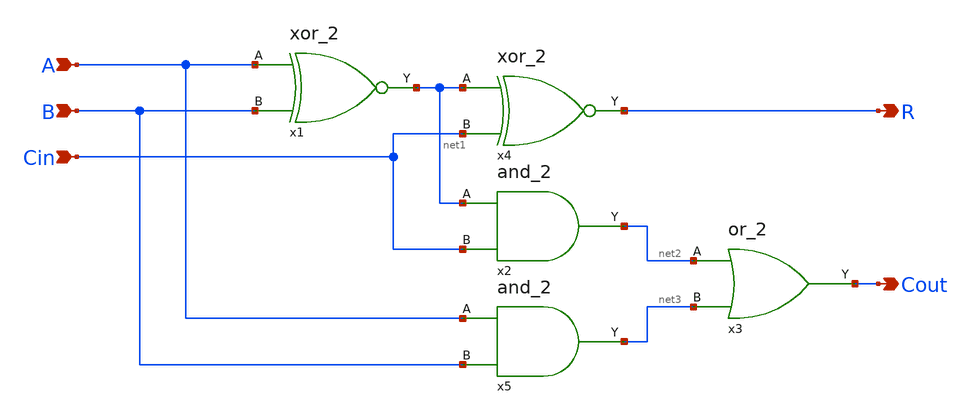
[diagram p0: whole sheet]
** sch_path: Circuiti/multiplier/full_adder.sch
**.subckt full_adder A B Cin R Cout
*.ipin A
*.ipin B
*.ipin Cin
*.opin R
*.opin Cout
x1 A net1 B xor_2
x2 net1 net2 Cin and_2
x3 net2 Cout net3 or_2
x4 net1 R Cin xor_2
x5 A net3 B and_2
**.ends

* expanding   symbol:  /home/matteo/Documenti/tesi/Circuiti/logic_gates_sch_sym/xor_2.sym # of
*+ pins=3
** sym_path: Circuiti/logic_gates_sch_sym/xor_2.sym
** sch_path: Circuiti/logic_gates_sch_sym/xor_2.sch
.subckt xor_2 A Y B
*.ipin A
*.ipin B
*.opin Y
x1 A net1 B nand_2
x2 A net2 B or_2
x3 net1 Y net2 and_2
.ends


* expanding   symbol:  /home/matteo/Documenti/tesi/Circuiti/logic_gates_sch_sym/and_2.sym # of
*+ pins=3
** sym_path: Circuiti/logic_gates_sch_sym/and_2.sym
** sch_path: Circuiti/logic_gates_sch_sym/and_2.sch
.subckt and_2 A Y B
*.ipin B
*.ipin A
*.opin Y
x1 A net1 B nand_2
x2 net1 Y not
.ends


* expanding   symbol:  /home/matteo/Documenti/tesi/Circuiti/logic_gates_sch_sym/or_2.sym # of pins=3
** sym_path: Circuiti/logic_gates_sch_sym/or_2.sym
** sch_path: Circuiti/logic_gates_sch_sym/or_2.sch
.subckt or_2 A Y B
*.ipin A
*.ipin B
*.opin Y
x1 A net1 B nor_2
x2 net1 Y not
.ends


* expanding   symbol:  /home/matteo/Documenti/tesi/Circuiti/logic_gates_sch_sym/nand_2.sym # of
*+ pins=3
** sym_path: Circuiti/logic_gates_sch_sym/nand_2.sym
** sch_path: Circuiti/logic_gates_sch_sym/nand_2.sch
.subckt nand_2 A Y B
*.ipin A
*.ipin B
*.opin Y
XM1 Y A net1 GND sky130_fd_pr__nfet_01v8 L=0.15 W=1 nf=1 ad='int((nf+1)/2) * W/nf * 0.29' as='int((nf+2)/2) * W/nf * 0.29'
+ pd='2*int((nf+1)/2) * (W/nf + 0.29)' ps='2*int((nf+2)/2) * (W/nf + 0.29)' nrd='0.29 / W' nrs='0.29 / W'
+ sa=0 sb=0 sd=0 mult=1 m=1
XM3 Y B Vdd VDD sky130_fd_pr__pfet_01v8 L=0.45 W=4.8 nf=1 ad='int((nf+1)/2) * W/nf * 0.29' as='int((nf+2)/2) * W/nf * 0.29'
+ pd='2*int((nf+1)/2) * (W/nf + 0.29)' ps='2*int((nf+2)/2) * (W/nf + 0.29)' nrd='0.29 / W' nrs='0.29 / W'
+ sa=0 sb=0 sd=0 mult=1 m=1
XM4 Y A Vdd VDD sky130_fd_pr__pfet_01v8 L=0.45 W=4.8 nf=1 ad='int((nf+1)/2) * W/nf * 0.29' as='int((nf+2)/2) * W/nf * 0.29'
+ pd='2*int((nf+1)/2) * (W/nf + 0.29)' ps='2*int((nf+2)/2) * (W/nf + 0.29)' nrd='0.29 / W' nrs='0.29 / W'
+ sa=0 sb=0 sd=0 mult=1 m=1
XM2 net1 B GND GND sky130_fd_pr__nfet_01v8 L=0.15 W=1 nf=1 ad='int((nf+1)/2) * W/nf * 0.29' as='int((nf+2)/2) * W/nf * 0.29'
+ pd='2*int((nf+1)/2) * (W/nf + 0.29)' ps='2*int((nf+2)/2) * (W/nf + 0.29)' nrd='0.29 / W' nrs='0.29 / W'
+ sa=0 sb=0 sd=0 mult=1 m=1
.ends


* expanding   symbol:  /home/matteo/Documenti/tesi/Circuiti/logic_gates_sch_sym/not.sym # of pins=2
** sym_path: Circuiti/logic_gates_sch_sym/not.sym
** sch_path: Circuiti/logic_gates_sch_sym/not.sch
.subckt not A Y
*.ipin A
*.opin Y
XM1 Y A GND GND sky130_fd_pr__nfet_01v8 L=0.45 W=1 nf=1 ad='int((nf+1)/2) * W/nf * 0.29' as='int((nf+2)/2) * W/nf * 0.29'
+ pd='2*int((nf+1)/2) * (W/nf + 0.29)' ps='2*int((nf+2)/2) * (W/nf + 0.29)' nrd='0.29 / W' nrs='0.29 / W'
+ sa=0 sb=0 sd=0 mult=1 m=1
XM2 Y A Vdd VDD sky130_fd_pr__pfet_01v8 L=0.45 W=4.8 nf=1 ad='int((nf+1)/2) * W/nf * 0.29' as='int((nf+2)/2) * W/nf * 0.29'
+ pd='2*int((nf+1)/2) * (W/nf + 0.29)' ps='2*int((nf+2)/2) * (W/nf + 0.29)' nrd='0.29 / W' nrs='0.29 / W'
+ sa=0 sb=0 sd=0 mult=1 m=1
.ends


* expanding   symbol:  /home/matteo/Documenti/tesi/Circuiti/logic_gates_sch_sym/nor_2.sym # of
*+ pins=3
** sym_path: Circuiti/logic_gates_sch_sym/nor_2.sym
** sch_path: Circuiti/logic_gates_sch_sym/nor_2.sch
.subckt nor_2 A Y B
*.opin Y
*.ipin A
*.ipin B
XM1 Y B GND GND sky130_fd_pr__nfet_01v8 L=0.45 W=1 nf=1 ad='int((nf+1)/2) * W/nf * 0.29' as='int((nf+2)/2) * W/nf * 0.29'
+ pd='2*int((nf+1)/2) * (W/nf + 0.29)' ps='2*int((nf+2)/2) * (W/nf + 0.29)' nrd='0.29 / W' nrs='0.29 / W'
+ sa=0 sb=0 sd=0 mult=1 m=1
XM3 Y B net1 VDD sky130_fd_pr__pfet_01v8 L=0.15 W=4.8 nf=1 ad='int((nf+1)/2) * W/nf * 0.29' as='int((nf+2)/2) * W/nf * 0.29'
+ pd='2*int((nf+1)/2) * (W/nf + 0.29)' ps='2*int((nf+2)/2) * (W/nf + 0.29)' nrd='0.29 / W' nrs='0.29 / W'
+ sa=0 sb=0 sd=0 mult=1 m=1
XM4 net1 A Vdd VDD sky130_fd_pr__pfet_01v8 L=0.15 W=4.8 nf=1 ad='int((nf+1)/2) * W/nf * 0.29' as='int((nf+2)/2) * W/nf * 0.29'
+ pd='2*int((nf+1)/2) * (W/nf + 0.29)' ps='2*int((nf+2)/2) * (W/nf + 0.29)' nrd='0.29 / W' nrs='0.29 / W'
+ sa=0 sb=0 sd=0 mult=1 m=1
XM2 Y A GND GND sky130_fd_pr__nfet_01v8 L=0.45 W=1 nf=1 ad='int((nf+1)/2) * W/nf * 0.29' as='int((nf+2)/2) * W/nf * 0.29'
+ pd='2*int((nf+1)/2) * (W/nf + 0.29)' ps='2*int((nf+2)/2) * (W/nf + 0.29)' nrd='0.29 / W' nrs='0.29 / W'
+ sa=0 sb=0 sd=0 mult=1 m=1
.ends

.GLOBAL Vdd
.GLOBAL GND
.end
